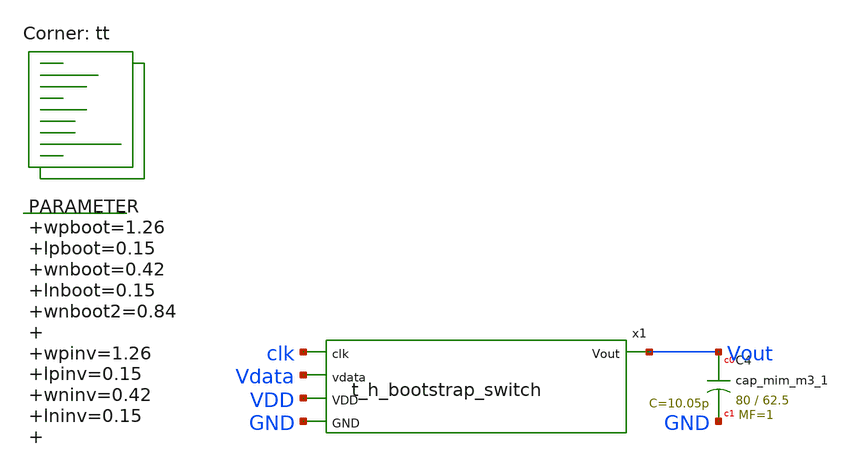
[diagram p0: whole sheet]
** sch_path: xschem/sample-n-hold-circuit-tb.sch
**.subckt sample-n-hold-circuit-tb
XC4 Vout GND sky130_fd_pr__cap_mim_m3_1 W=80 L=62.5 MF=1 m=1
x1 clk Vdata VDD GND Vout t_h_bootstrap_switch
.param wpboot=1.26 lpboot=0.15 wnboot=0.42 lnboot=0.15 wnboot2=0.84 wpinv=1.26 lpinv=0.15 wninv=0.42
+ lninv=0.15 wcboot=8 lcboot=6.25 wnsw=5 lnsw=0.3 wnsw2=1 wpsw=2


**** begin user architecture code
 .lib $::SKYWATER_MODELS/sky130.lib.spice tt
.include $::SKYWATER_STDCELLS/sky130_fd_sc_hd.spice
.param mc_mm_switch = 0
.param mc_pr_switch = 0




  .param fin=10e3
  .param fclk={fin*10} tclk={1/fclk} thclk={tclk/2}
  .option wnflag=1
  .option safecurrents

  Vvdd vdd   gnd 1.8
  Vdt  vdata gnd sin(0.5 0.5 9.3e3 10e-9)
  Vclk clk   gnd pulse(0 1.8 10e-9 1p 1p {thclk} {tclk})

  .control
    reset
    save all
    tran 10n 1m
    write sample-n-hold-circuit-tb.raw
    quit 0
  .endc



**** end user architecture code
**.ends

* expanding   symbol:  t_h_bootstrap_switch.sym # of pins=5
** sym_path: xschem/t_h_bootstrap_switch.sym
** sch_path: xschem/t_h_bootstrap_switch.sch
.subckt t_h_bootstrap_switch clk vdata VDD GND Vout
*.ipin clk
*.opin Vout
*.ipin vdata
*.ipin VDD
*.ipin GND
XM1 VDD boot2 boot1 GND sky130_fd_pr__nfet_01v8 L=lnboot W=wnboot nf=1 ad='int((nf+1)/2) * W/nf * 0.29'
+ as='int((nf+2)/2) * W/nf * 0.29' pd='2*int((nf+1)/2) * (W/nf + 0.29)' ps='2*int((nf+2)/2) * (W/nf + 0.29)'
+ nrd='0.29 / W' nrs='0.29 / W' sa=0 sb=0 sd=0 mult=1 m=1
XM2 Vboot net3 net1 net1 sky130_fd_pr__pfet_01v8 L=lpboot W=wpsw nf=1 ad='int((nf+1)/2) * W/nf * 0.29'
+ as='int((nf+2)/2) * W/nf * 0.29' pd='2*int((nf+1)/2) * (W/nf + 0.29)' ps='2*int((nf+2)/2) * (W/nf + 0.29)'
+ nrd='0.29 / W' nrs='0.29 / W' sa=0 sb=0 sd=0 mult=1 m=1
XC1 boot1 clkb sky130_fd_pr__cap_mim_m3_1 W=8 L=6.25 MF=1 m=1
XC2 boot2 clkboot sky130_fd_pr__cap_mim_m3_1 W=8 L=6.25 MF=1 m=1
XM4 VDD boot1 net1 GND sky130_fd_pr__nfet_01v8 L=lnboot W=wnboot2 nf=1 ad='int((nf+1)/2) * W/nf * 0.29'
+ as='int((nf+2)/2) * W/nf * 0.29' pd='2*int((nf+1)/2) * (W/nf + 0.29)' ps='2*int((nf+2)/2) * (W/nf + 0.29)'
+ nrd='0.29 / W' nrs='0.29 / W' sa=0 sb=0 sd=0 mult=1 m=1
XM5 net2 clkb GND GND sky130_fd_pr__nfet_01v8 L=lnboot W=wnboot nf=1 ad='int((nf+1)/2) * W/nf * 0.29'
+ as='int((nf+2)/2) * W/nf * 0.29' pd='2*int((nf+1)/2) * (W/nf + 0.29)' ps='2*int((nf+2)/2) * (W/nf + 0.29)'
+ nrd='0.29 / W' nrs='0.29 / W' sa=0 sb=0 sd=0 mult=1 m=1
XC3 net1 net2 sky130_fd_pr__cap_mim_m3_1 W=25 L=20 MF=1 m=1
XM6 net3 clkboot VDD VDD sky130_fd_pr__pfet_01v8 L=lpinv W=wpinv nf=1 ad='int((nf+1)/2) * W/nf * 0.29'
+ as='int((nf+2)/2) * W/nf * 0.29' pd='2*int((nf+1)/2) * (W/nf + 0.29)' ps='2*int((nf+2)/2) * (W/nf + 0.29)'
+ nrd='0.29 / W' nrs='0.29 / W' sa=0 sb=0 sd=0 mult=1 m=1
XM7 net3 clkboot net2 GND sky130_fd_pr__nfet_01v8 L=lninv W=wninv nf=1 ad='int((nf+1)/2) * W/nf * 0.29'
+ as='int((nf+2)/2) * W/nf * 0.29' pd='2*int((nf+1)/2) * (W/nf + 0.29)' ps='2*int((nf+2)/2) * (W/nf + 0.29)'
+ nrd='0.29 / W' nrs='0.29 / W' sa=0 sb=0 sd=0 mult=1 m=1
XM8 Vboot VDD net4 GND sky130_fd_pr__nfet_01v8 L=lnboot W=wnboot nf=1 ad='int((nf+1)/2) * W/nf * 0.29'
+ as='int((nf+2)/2) * W/nf * 0.29' pd='2*int((nf+1)/2) * (W/nf + 0.29)' ps='2*int((nf+2)/2) * (W/nf + 0.29)'
+ nrd='0.29 / W' nrs='0.29 / W' sa=0 sb=0 sd=0 mult=1 m=1
XM9 net4 clkb GND GND sky130_fd_pr__nfet_01v8 L=lnboot W=wnboot nf=1 ad='int((nf+1)/2) * W/nf * 0.29'
+ as='int((nf+2)/2) * W/nf * 0.29' pd='2*int((nf+1)/2) * (W/nf + 0.29)' ps='2*int((nf+2)/2) * (W/nf + 0.29)'
+ nrd='0.29 / W' nrs='0.29 / W' sa=0 sb=0 sd=0 mult=1 m=1
XM10 net3 Vboot net2 GND sky130_fd_pr__nfet_01v8 L=lnboot W=wnboot nf=1 ad='int((nf+1)/2) * W/nf * 0.29'
+ as='int((nf+2)/2) * W/nf * 0.29' pd='2*int((nf+1)/2) * (W/nf + 0.29)' ps='2*int((nf+2)/2) * (W/nf + 0.29)'
+ nrd='0.29 / W' nrs='0.29 / W' sa=0 sb=0 sd=0 mult=1 m=1
XM11 vdata Vboot net2 GND sky130_fd_pr__nfet_01v8 L=lnboot W=wnsw2 nf=1 ad='int((nf+1)/2) * W/nf * 0.29'
+ as='int((nf+2)/2) * W/nf * 0.29' pd='2*int((nf+1)/2) * (W/nf + 0.29)' ps='2*int((nf+2)/2) * (W/nf + 0.29)'
+ nrd='0.29 / W' nrs='0.29 / W' sa=0 sb=0 sd=0 mult=1 m=1
XM12 Vout Vboot vdata GND sky130_fd_pr__nfet_01v8 L=lnsw W=wnsw nf=1 ad='int((nf+1)/2) * W/nf * 0.29'
+ as='int((nf+2)/2) * W/nf * 0.29' pd='2*int((nf+1)/2) * (W/nf + 0.29)' ps='2*int((nf+2)/2) * (W/nf + 0.29)'
+ nrd='0.29 / W' nrs='0.29 / W' sa=0 sb=0 sd=0 mult=1 m=1
XM13 clkb clk VDD VDD sky130_fd_pr__pfet_01v8 L=lpinv W=wpinv nf=1 ad='int((nf+1)/2) * W/nf * 0.29' as='int((nf+2)/2) * W/nf * 0.29'
+ pd='2*int((nf+1)/2) * (W/nf + 0.29)' ps='2*int((nf+2)/2) * (W/nf + 0.29)' nrd='0.29 / W' nrs='0.29 / W'
+ sa=0 sb=0 sd=0 mult=1 m=1
XM14 clkb clk GND GND sky130_fd_pr__nfet_01v8 L=lninv W=wninv nf=1 ad='int((nf+1)/2) * W/nf * 0.29' as='int((nf+2)/2) * W/nf * 0.29'
+ pd='2*int((nf+1)/2) * (W/nf + 0.29)' ps='2*int((nf+2)/2) * (W/nf + 0.29)' nrd='0.29 / W' nrs='0.29 / W'
+ sa=0 sb=0 sd=0 mult=1 m=1
XM15 clkboot clkb VDD VDD sky130_fd_pr__pfet_01v8 L=lpinv W=wpinv nf=1 ad='int((nf+1)/2) * W/nf * 0.29'
+ as='int((nf+2)/2) * W/nf * 0.29' pd='2*int((nf+1)/2) * (W/nf + 0.29)' ps='2*int((nf+2)/2) * (W/nf + 0.29)'
+ nrd='0.29 / W' nrs='0.29 / W' sa=0 sb=0 sd=0 mult=1 m=1
XM16 clkboot clkb GND GND sky130_fd_pr__nfet_01v8 L=lninv W=wninv nf=1 ad='int((nf+1)/2) * W/nf * 0.29'
+ as='int((nf+2)/2) * W/nf * 0.29' pd='2*int((nf+1)/2) * (W/nf + 0.29)' ps='2*int((nf+2)/2) * (W/nf + 0.29)'
+ nrd='0.29 / W' nrs='0.29 / W' sa=0 sb=0 sd=0 mult=1 m=1
XM3 VDD boot1 boot2 GND sky130_fd_pr__nfet_01v8 L=lnboot W=wnboot nf=1 ad='int((nf+1)/2) * W/nf * 0.29'
+ as='int((nf+2)/2) * W/nf * 0.29' pd='2*int((nf+1)/2) * (W/nf + 0.29)' ps='2*int((nf+2)/2) * (W/nf + 0.29)'
+ nrd='0.29 / W' nrs='0.29 / W' sa=0 sb=0 sd=0 mult=1 m=1
.ends

.end
